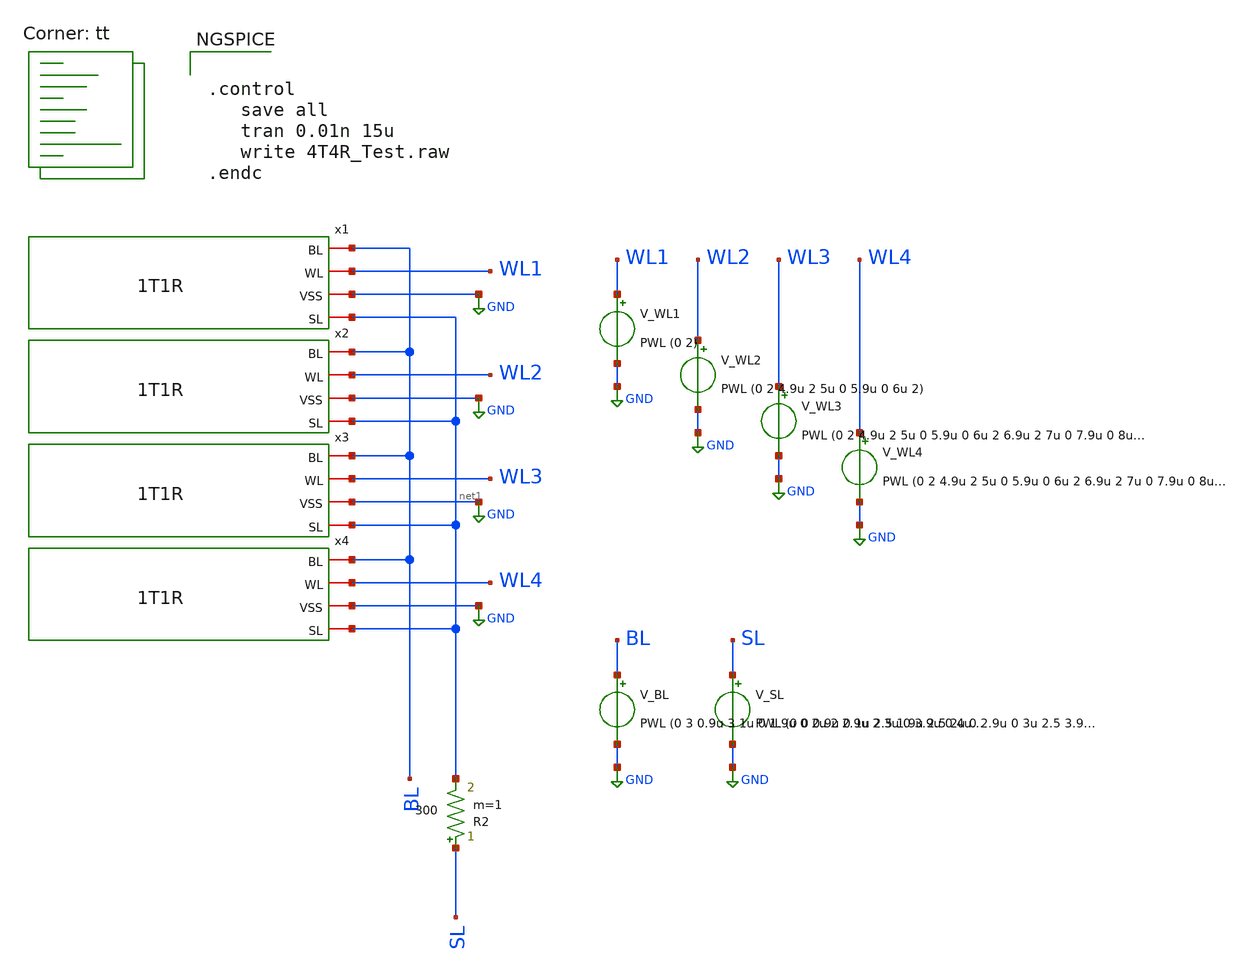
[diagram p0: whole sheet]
** sch_path: xschem/test/xschem/4T4R_Test.sch
* StefanSchippers/xschem_sky130/sky130_fd_pr/reram.sym:
* Copyright 2021 Stefan Frederik Schippers
* Licensed under the Apache License, Version 2.0 (the "License");
**.subckt 4T4R_Test
x1 BL WL1 net1 GND 1T1R
x2 BL WL2 net1 GND 1T1R
x3 BL WL3 net1 GND 1T1R
x4 BL WL4 net1 GND 1T1R
V_WL1 WL1 GND PWL (0 2)
V_WL2 WL2 GND PWL (0 2 4.9u 2 5u 0 5.9u 0 6u 2)
V_WL3 WL3 GND PWL (0 2 4.9u 2 5u 0 5.9u 0 6u 2 6.9u 2 7u 0 7.9u 0 8u 2)
V_WL4 WL4 GND PWL (0 2 4.9u 2 5u 0 5.9u 0 6u 2 6.9u 2 7u 0 7.9u 0 8u 2 8.9u 2 9u 0 9.9u 0 10u 2)
V_SL SL GND PWL (0 0 0.9u 0 1u 2.5 1.9u 2.5 2u 0 2.9u 0 3u 2.5 3.9u 2.5 4u 0)
V_BL BL GND PWL (0 3 0.9u 3 1u 0 1.9u 0 2u 2 2.9u 2 3u 0 3.9u 0 4u 0.2 4.9u 0.2 5u 2 5.9u 2 6u 0.2
+ 6.9u 0.2 7u 2 7.9u 2 8u 0.2 8.9u 0.2 9u 2 9.9u 2 10u 0.2 10.9u 0.2 11u 2 11.9u 2 12u 0.2)
R2 SL net1 300 m=1
**** begin user architecture code
.lib $::SKYWATER_MODELS/sky130.lib.spice tt


.control
   save all
   tran 0.01n 15u
   write 4T4R_Test.raw
.endc


**** end user architecture code
**.ends

* expanding   symbol:  1T1R.sym # of pins=4
** sym_path: xschem/test/xschem/1T1R.sym
** sch_path: xschem/test/xschem/1T1R.sch
.subckt 1T1R BL WL SL VSS
*.iopin SL
*.iopin WL
*.iopin BL
*.iopin VSS
XR1 BL net1 sky130_fd_pr_reram__reram_cell Tfilament_0=3.8e-9
XM1 net1 WL SL VSS sky130_fd_pr__nfet_g5v0d10v5 L=0.5 W=7 nf=1 ad='int((nf+1)/2) * W/nf * 0.29' as='int((nf+2)/2) * W/nf * 0.29'
+ pd='2*int((nf+1)/2) * (W/nf + 0.29)' ps='2*int((nf+2)/2) * (W/nf + 0.29)' nrd='0.29 / W' nrs='0.29 / W'
+ sa=0 sb=0 sd=0 mult=1 m=1
.ends

.GLOBAL GND
**** begin user architecture code

.subckt sky130_fd_pr_reram__reram_cell TE BE Tfilament_0=3.3e-9 area_ox=0.1024e-12
N1 TE BE nFilament sky130_fd_pr_reram__reram_model
.ic v(nFilament)={Tfilament_0*1.0e9}
.ends sky130_fd_pr_reram__reram_cell

.model sky130_fd_pr_reram__reram_model sky130_fd_pr_reram__reram_module  area_ox = 0.1024e-12  Tox =
+ 5.0  Tfilament_max = 4.9  Tfilament_min = 3.3  Eact_generation = 1.501  Eact_recombination  = 1.500
+  I_k1  = 6.140e-5  Tfilament_ref = 4.7249  V_ref = 0.430  velocity_k1 = 150  gamma_k0  = 16.5  gamma_k1
+  = -1.25  Temperature_0 = 300  C_thermal = 3.1825e-16  tau_thermal = 0.23e-9  t_step  = 1.0e-9
+  smoothing = 1e-7  Kclip = 200

.control
pre_osdi $SKYWATER_MODELS/sky130_fd_pr_reram__reram_module.osdi
.endc

**** end user architecture code
.end
